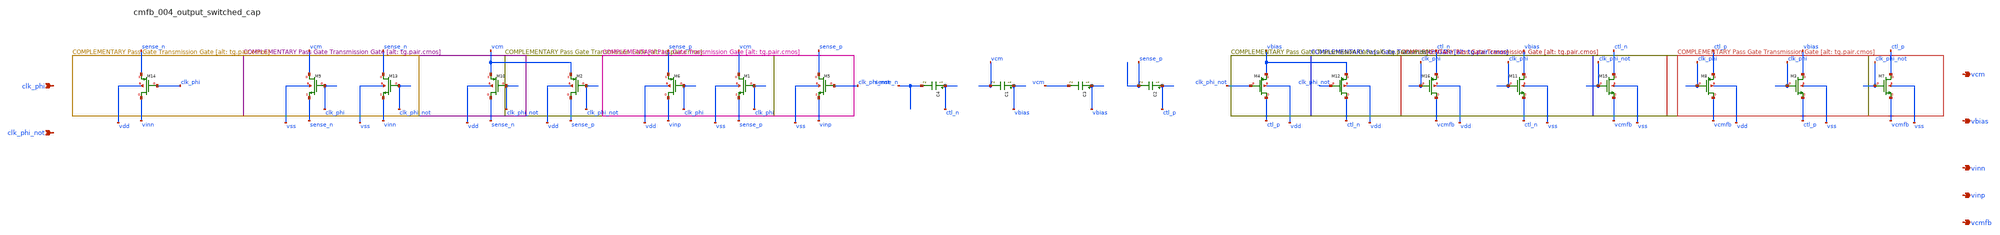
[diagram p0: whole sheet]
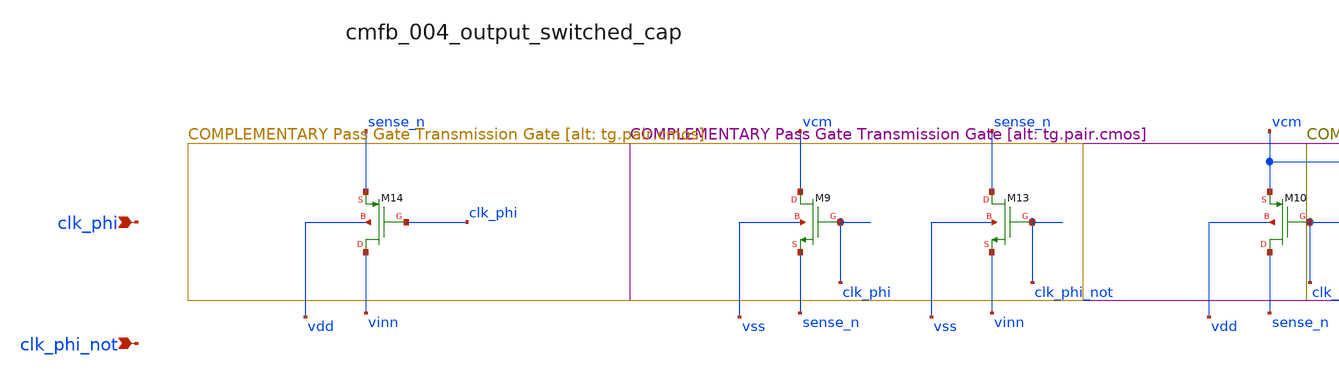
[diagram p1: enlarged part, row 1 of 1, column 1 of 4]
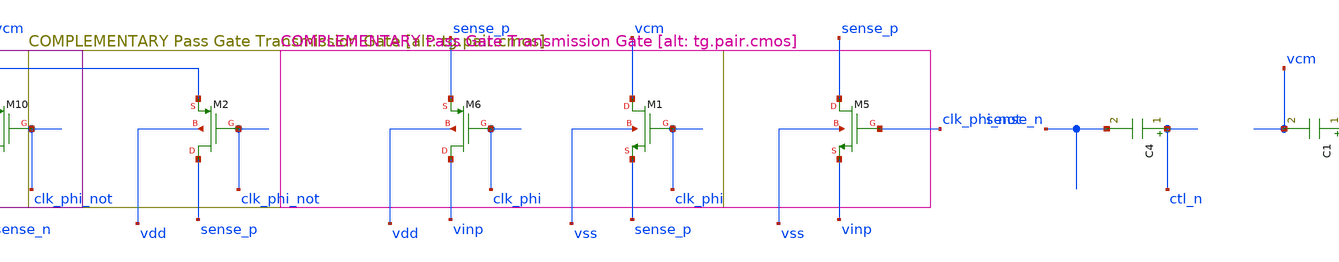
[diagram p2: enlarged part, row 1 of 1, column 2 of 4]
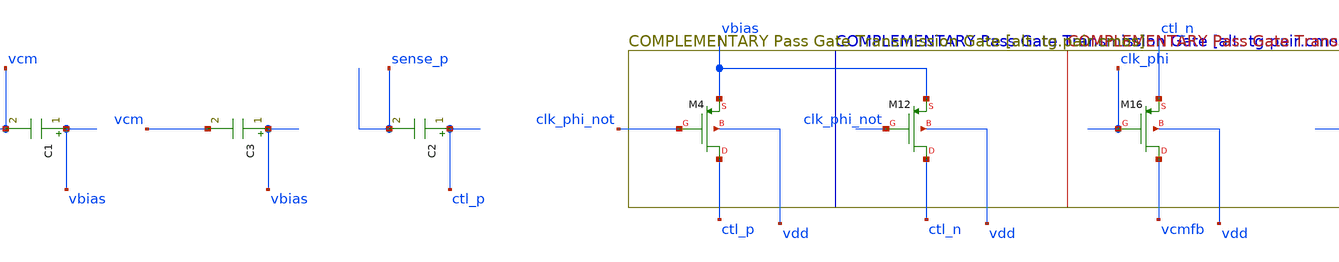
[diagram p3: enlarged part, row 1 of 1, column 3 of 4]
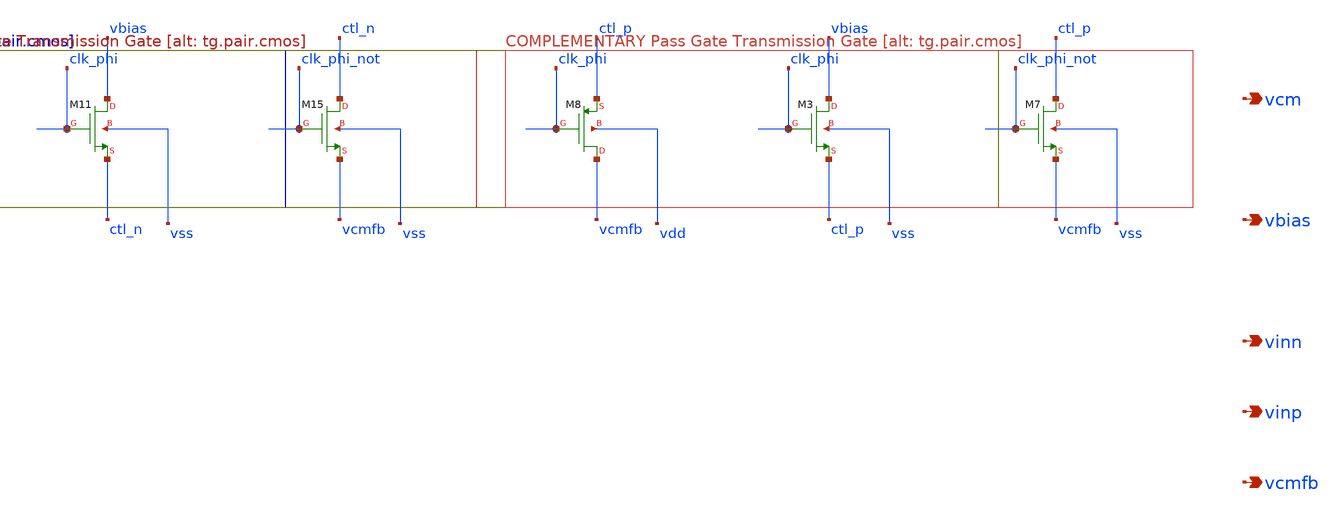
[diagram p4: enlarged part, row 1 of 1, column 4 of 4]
** sch_path: analog-db/raw/cmfb_004_output_switched_cap/cmfb_004_output_switched_cap_annotated.sch
**.subckt cmfb_004_output_switched_cap_annotated clk_phi clk_phi_not vcm vbias vinn vinp vcmfb
*.ipin clk_phi
*.ipin clk_phi_not
*.opin vcm
*.opin vbias
*.opin vinn
*.opin vinp
*.opin vcmfb
C1 vbias vcm 'x_dut_c1_value' m=1
C2 ctl_p sense_p 'x_dut_c2_value' m=1
C3 vbias vcm 'x_dut_c3_value' m=1
C4 ctl_n sense_n 'x_dut_c4_value' m=1
XM1 vcm clk_phi sense_p vss sg13_lv_nmos w=x_dut_xm1_w l=x_dut_xm1_l ng=1 m=x_dut_xm1_m
XM10 sense_n clk_phi_not vcm vdd sg13_lv_pmos w=x_dut_xm10_w l=x_dut_xm10_l ng=1 m=x_dut_xm10_m
XM11 vbias clk_phi ctl_n vss sg13_lv_nmos w=x_dut_xm11_w l=x_dut_xm11_l ng=1 m=x_dut_xm11_m
XM12 ctl_n clk_phi_not vbias vdd sg13_lv_pmos w=x_dut_xm12_w l=x_dut_xm12_l ng=1 m=x_dut_xm12_m
XM13 sense_n clk_phi_not vinn vss sg13_lv_nmos w=x_dut_xm13_w l=x_dut_xm13_l ng=1 m=x_dut_xm13_m
XM14 vinn clk_phi sense_n vdd sg13_lv_pmos w=x_dut_xm14_w l=x_dut_xm14_l ng=1 m=x_dut_xm14_m
XM15 ctl_n clk_phi_not vcmfb vss sg13_lv_nmos w=x_dut_xm15_w l=x_dut_xm15_l ng=1 m=x_dut_xm15_m
XM16 vcmfb clk_phi ctl_n vdd sg13_lv_pmos w=x_dut_xm16_w l=x_dut_xm16_l ng=1 m=x_dut_xm16_m
XM2 sense_p clk_phi_not vcm vdd sg13_lv_pmos w=x_dut_xm2_w l=x_dut_xm2_l ng=1 m=x_dut_xm2_m
XM3 vbias clk_phi ctl_p vss sg13_lv_nmos w=x_dut_xm3_w l=x_dut_xm3_l ng=1 m=x_dut_xm3_m
XM4 ctl_p clk_phi_not vbias vdd sg13_lv_pmos w=x_dut_xm4_w l=x_dut_xm4_l ng=1 m=x_dut_xm4_m
XM5 sense_p clk_phi_not vinp vss sg13_lv_nmos w=x_dut_xm5_w l=x_dut_xm5_l ng=1 m=x_dut_xm5_m
XM6 vinp clk_phi sense_p vdd sg13_lv_pmos w=x_dut_xm6_w l=x_dut_xm6_l ng=1 m=x_dut_xm6_m
XM7 ctl_p clk_phi_not vcmfb vss sg13_lv_nmos w=x_dut_xm7_w l=x_dut_xm7_l ng=1 m=x_dut_xm7_m
XM8 vcmfb clk_phi ctl_p vdd sg13_lv_pmos w=x_dut_xm8_w l=x_dut_xm8_l ng=1 m=x_dut_xm8_m
XM9 vcm clk_phi sense_n vss sg13_lv_nmos w=x_dut_xm9_w l=x_dut_xm9_l ng=1 m=x_dut_xm9_m
**.ends
.end
